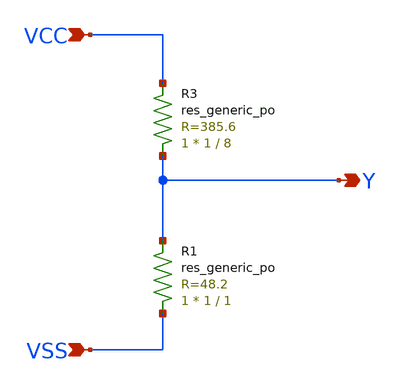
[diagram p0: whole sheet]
** sch_path: xschem/vDivider_02.sch
**.subckt vDivider_02 VCC VSS Y
*.ipin VCC
*.ipin VSS
*.opin Y
XR3 Y VCC sky130_fd_pr__res_generic_po W=1 L=8 m=1
XR1 VSS Y sky130_fd_pr__res_generic_po W=1 L=1 m=1
**.ends
.end
